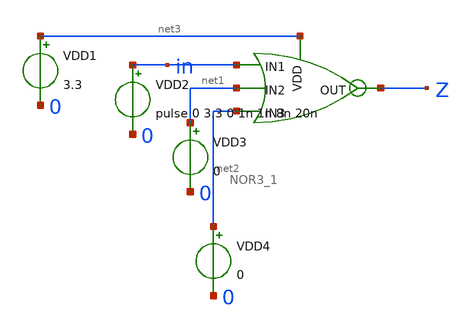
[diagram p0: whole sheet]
** sch_path: chipathon_2023/initial_notebooks_2023/accepted_notebooks/Current-Steering-DAC/DAC/Test_NOR3_1.sch
**.subckt Test_NOR3_1
VDD1 net3 0 3.3
VDD2 in 0 pulse 0 3.3 0 1n 1n 8n 20n
VDD3 net1 0 0
VDD4 net2 0 0
x1 net3 in net1 Z net2 NOR3_1
**** begin user architecture code




.include /foss/pdks/gf180mcuC/libs.tech/ngspice/design.ngspice
.lib /foss/pdks/gf180mcuC/libs.tech/ngspice/sm141064.ngspice typical


.control
	tran 0.1n 50n
	*dc vin1 0 3.3 0.1
	plot v(in) v(Z)
	*plot v(vout)
.endc
.save all




**** end user architecture code
**.ends
.end
